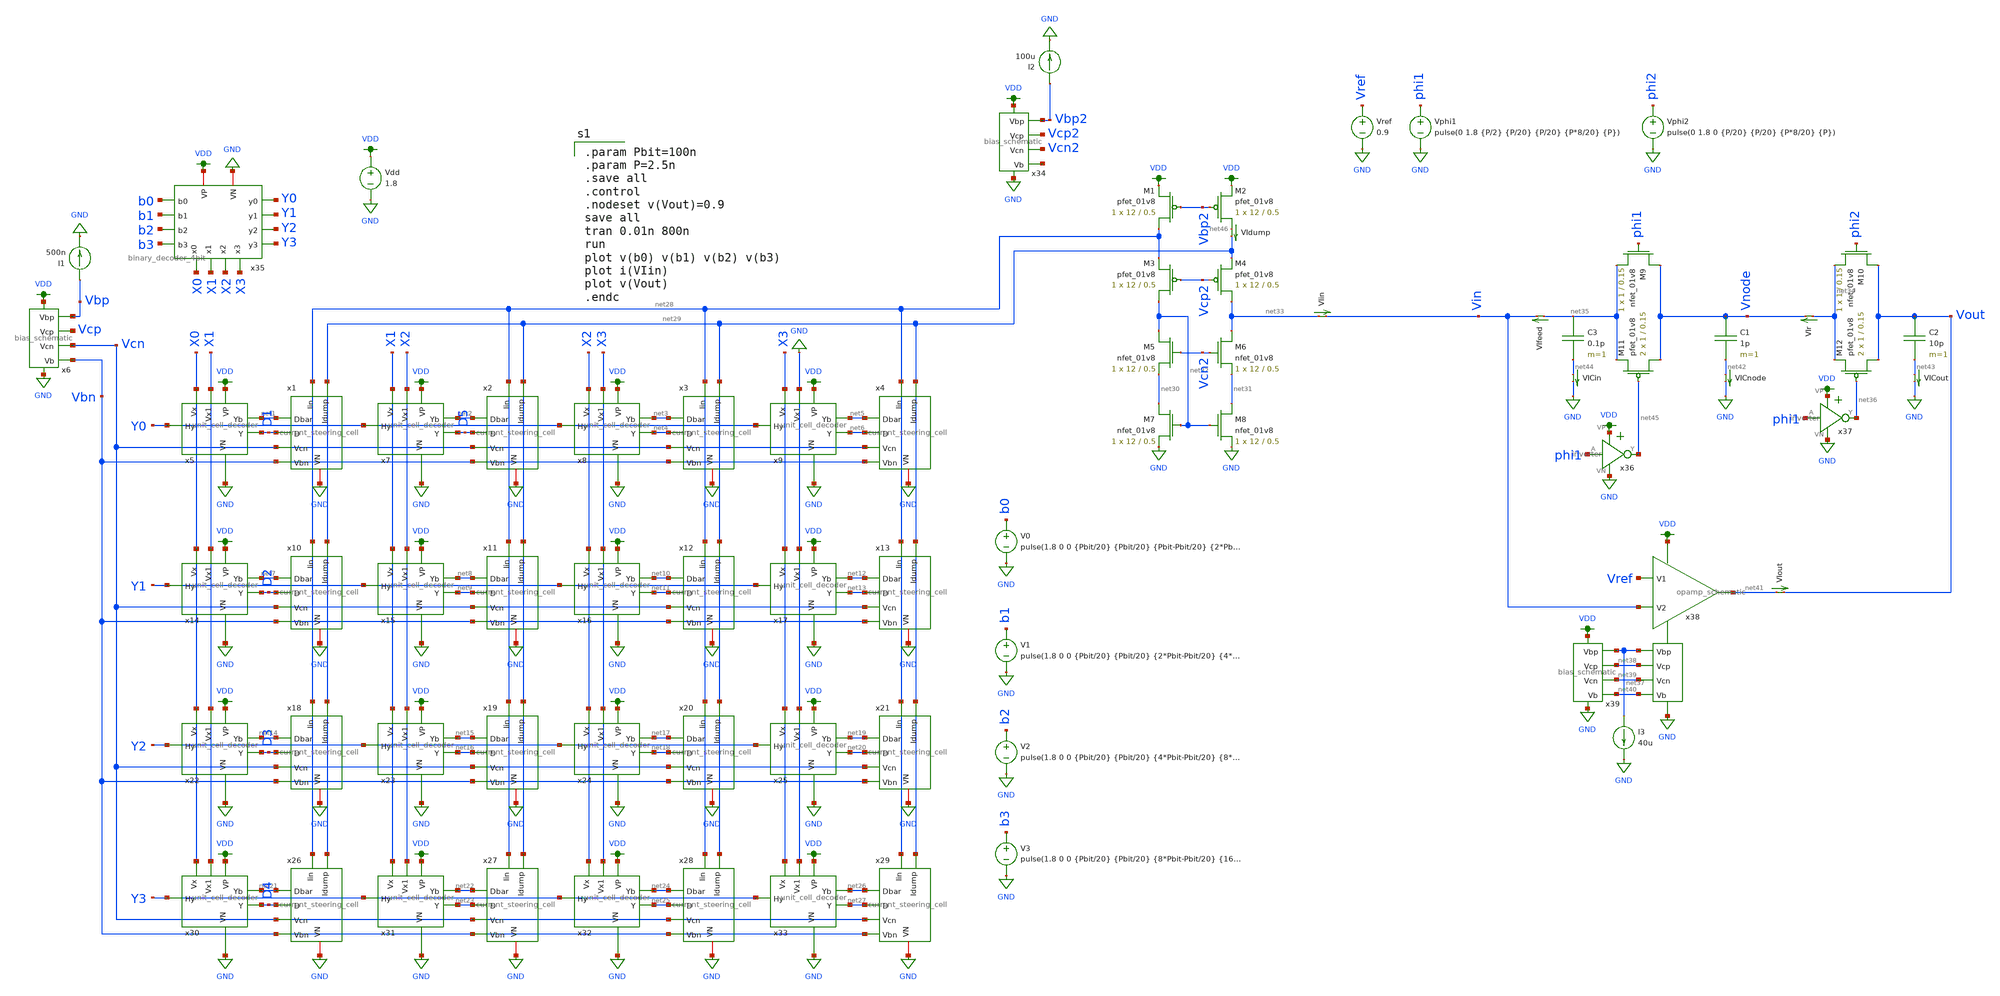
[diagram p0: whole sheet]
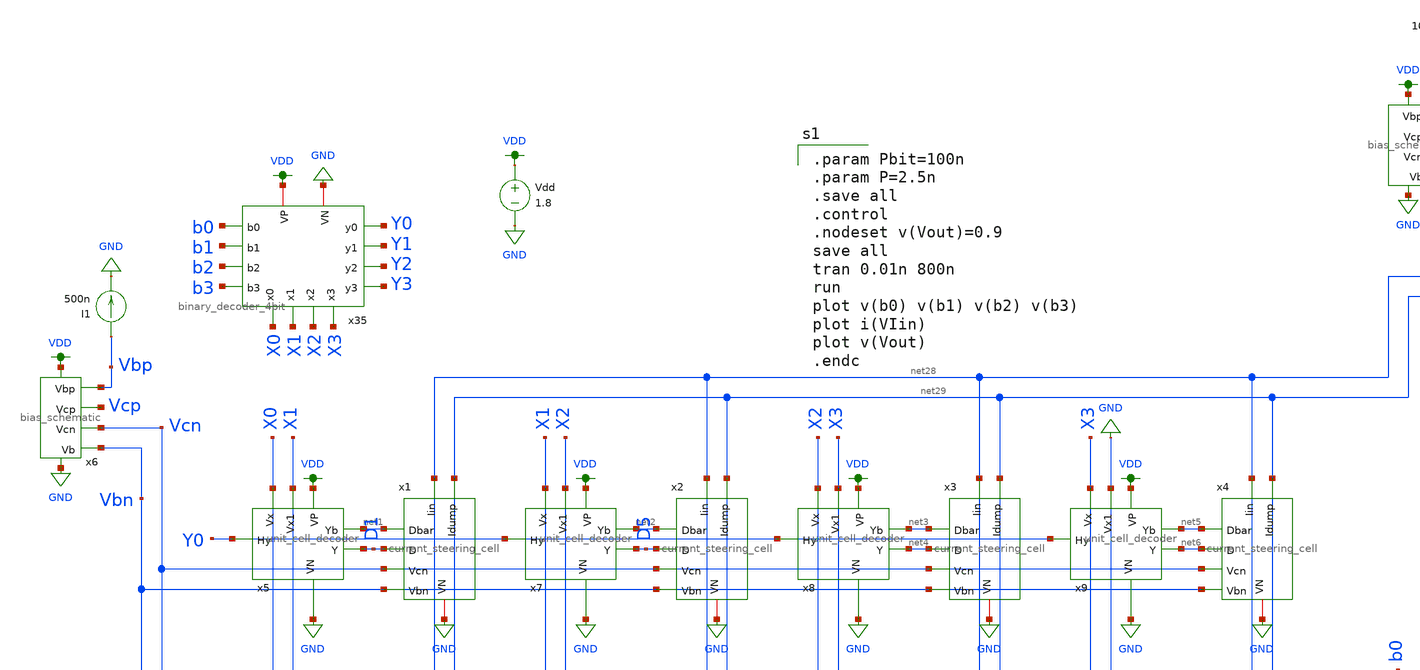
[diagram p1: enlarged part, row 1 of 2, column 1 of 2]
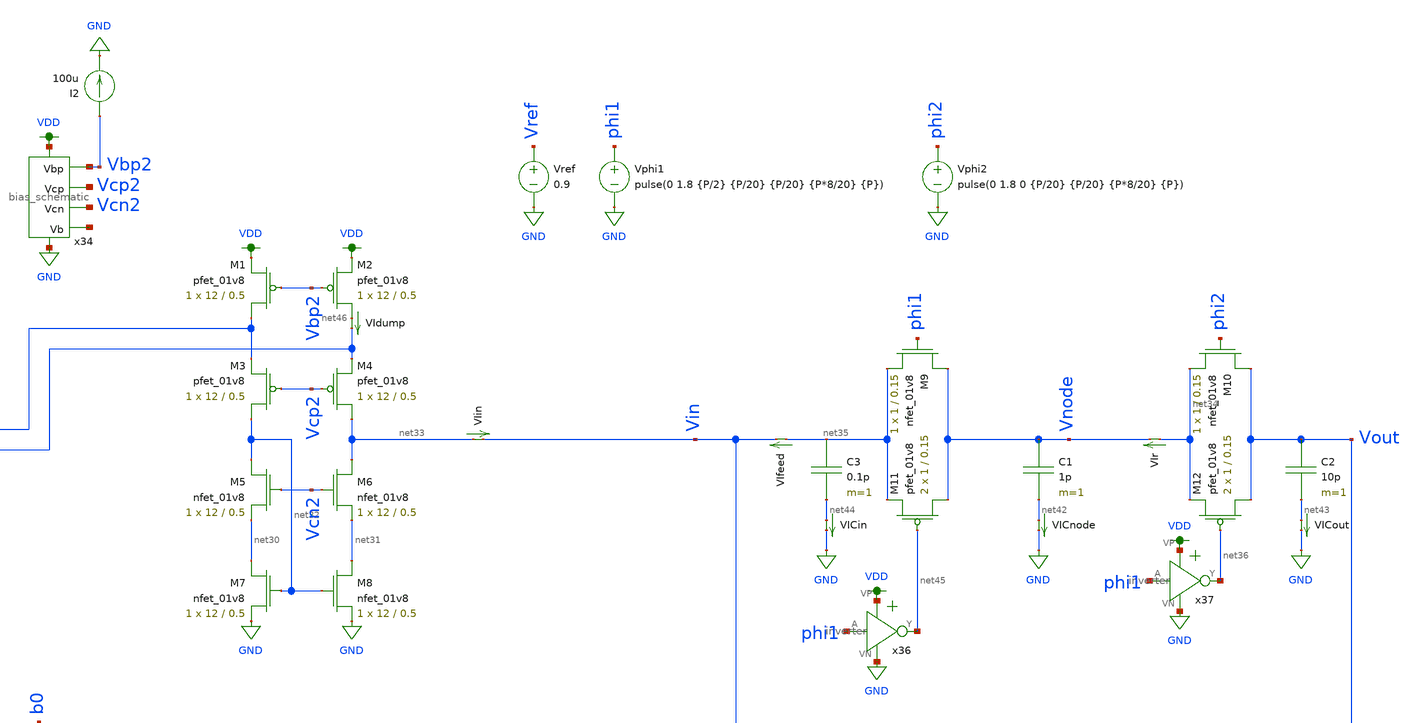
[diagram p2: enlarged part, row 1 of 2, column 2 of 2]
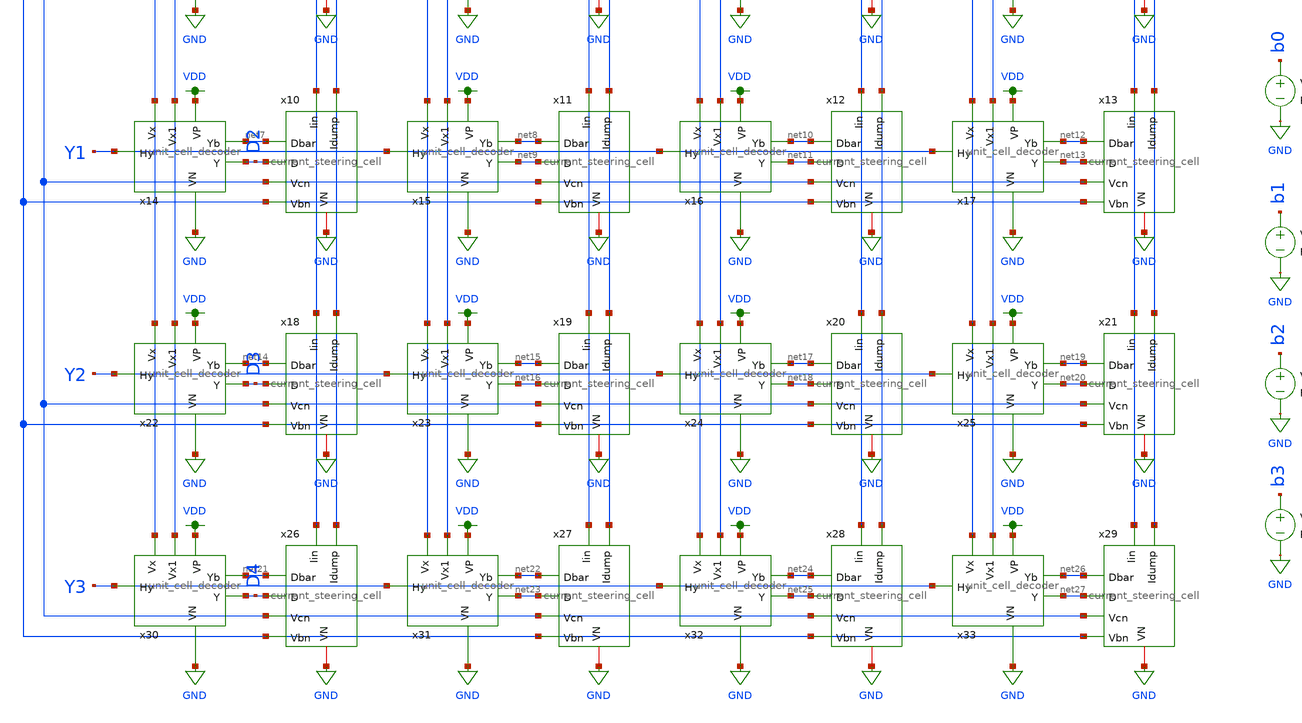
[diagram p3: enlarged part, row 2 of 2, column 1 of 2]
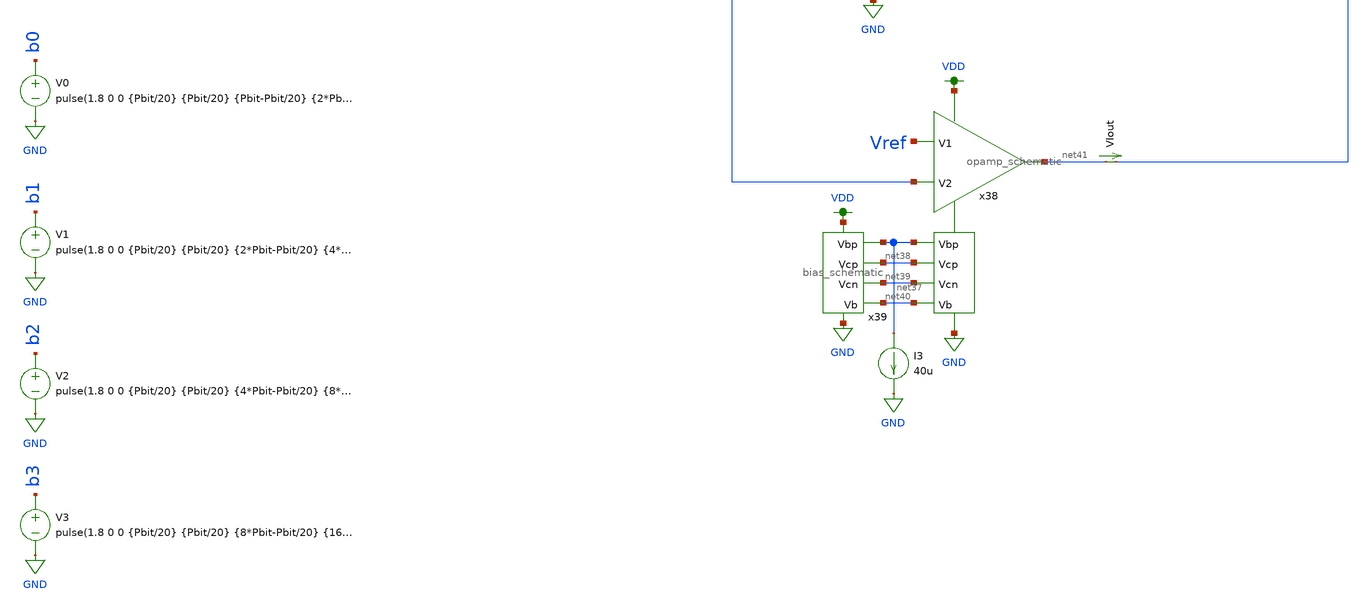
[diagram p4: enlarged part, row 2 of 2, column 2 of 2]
** sch_path: xschem/current_steering_testbenches/current_steering_testbench_transient_sciv.sch
**.subckt current_steering_testbench_transient_sciv
V1 b1 GND pulse(1.8 0 0 {Pbit/20} {Pbit/20} {2*Pbit-Pbit/20} {4*Pbit}
V2 b2 GND pulse(1.8 0 0 {Pbit/20} {Pbit/20} {4*Pbit-Pbit/20} {8*Pbit}
V3 b3 GND pulse(1.8 0 0 {Pbit/20} {Pbit/20} {8*Pbit-Pbit/20} {16*Pbit}
I1 Vbp GND 500n
VIin net33 Vin 0
.save i(viin)
Vdd VDD GND 1.8
XM1 net28 Vbp2 VDD VDD sky130_fd_pr__pfet_01v8 L=0.5 W=12 nf=1 ad='int((nf+1)/2) * W/nf * 0.29' as='int((nf+2)/2) * W/nf * 0.29'
+ pd='2*int((nf+1)/2) * (W/nf + 0.29)' ps='2*int((nf+2)/2) * (W/nf + 0.29)' nrd='0.29 / W' nrs='0.29 / W'
+ sa=0 sb=0 sd=0 mult=1 m=1
XM2 net46 Vbp2 VDD VDD sky130_fd_pr__pfet_01v8 L=0.5 W=12 nf=1 ad='int((nf+1)/2) * W/nf * 0.29' as='int((nf+2)/2) * W/nf * 0.29'
+ pd='2*int((nf+1)/2) * (W/nf + 0.29)' ps='2*int((nf+2)/2) * (W/nf + 0.29)' nrd='0.29 / W' nrs='0.29 / W'
+ sa=0 sb=0 sd=0 mult=1 m=1
XM3 net32 Vcp2 net28 VDD sky130_fd_pr__pfet_01v8 L=0.5 W=12 nf=1 ad='int((nf+1)/2) * W/nf * 0.29' as='int((nf+2)/2) * W/nf * 0.29'
+ pd='2*int((nf+1)/2) * (W/nf + 0.29)' ps='2*int((nf+2)/2) * (W/nf + 0.29)' nrd='0.29 / W' nrs='0.29 / W'
+ sa=0 sb=0 sd=0 mult=1 m=1
XM4 net33 Vcp2 net29 VDD sky130_fd_pr__pfet_01v8 L=0.5 W=12 nf=1 ad='int((nf+1)/2) * W/nf * 0.29' as='int((nf+2)/2) * W/nf * 0.29'
+ pd='2*int((nf+1)/2) * (W/nf + 0.29)' ps='2*int((nf+2)/2) * (W/nf + 0.29)' nrd='0.29 / W' nrs='0.29 / W'
+ sa=0 sb=0 sd=0 mult=1 m=1
V0 b0 GND pulse(1.8 0 0 {Pbit/20} {Pbit/20} {Pbit-Pbit/20} {2*Pbit}
x5 X0 X1 Y0 VDD GND net1 D1 unit_cell_decoder
x7 X1 X2 Y0 VDD GND net2 D5 unit_cell_decoder
x8 X2 X3 Y0 VDD GND net3 net4 unit_cell_decoder
x9 X3 GND Y0 VDD GND net5 net6 unit_cell_decoder
x14 X0 X1 Y1 VDD GND net7 D2 unit_cell_decoder
x15 X1 X2 Y1 VDD GND net8 net9 unit_cell_decoder
x16 X2 X3 Y1 VDD GND net10 net11 unit_cell_decoder
x17 X3 GND Y1 VDD GND net12 net13 unit_cell_decoder
x22 X0 X1 Y2 VDD GND net14 D3 unit_cell_decoder
x23 X1 X2 Y2 VDD GND net15 net16 unit_cell_decoder
x24 X2 X3 Y2 VDD GND net17 net18 unit_cell_decoder
x25 X3 GND Y2 VDD GND net19 net20 unit_cell_decoder
x30 X0 X1 Y3 VDD GND net21 D4 unit_cell_decoder
x31 X1 X2 Y3 VDD GND net22 net23 unit_cell_decoder
x32 X2 X3 Y3 VDD GND net24 net25 unit_cell_decoder
x33 X3 GND Y3 VDD GND net26 net27 unit_cell_decoder
x1 net28 net29 net1 D1 Vcn Vbn GND current_steering_cell
x2 net28 net29 net2 D5 Vcn Vbn GND current_steering_cell
x3 net28 net29 net3 net4 Vcn Vbn GND current_steering_cell
x4 net28 net29 net5 net6 Vcn Vbn GND current_steering_cell
x10 net28 net29 net7 D2 Vcn Vbn GND current_steering_cell
x11 net28 net29 net8 net9 Vcn Vbn GND current_steering_cell
x12 net28 net29 net10 net11 Vcn Vbn GND current_steering_cell
x13 net28 net29 net12 net13 Vcn Vbn GND current_steering_cell
x18 net28 net29 net14 D3 Vcn Vbn GND current_steering_cell
x19 net28 net29 net15 net16 Vcn Vbn GND current_steering_cell
x20 net28 net29 net17 net18 Vcn Vbn GND current_steering_cell
x21 net28 net29 net19 net20 Vcn Vbn GND current_steering_cell
x26 net28 net29 net21 D4 Vcn Vbn GND current_steering_cell
x27 net28 net29 net22 net23 Vcn Vbn GND current_steering_cell
x28 net28 net29 net24 net25 Vcn Vbn GND current_steering_cell
x29 net28 net29 net26 net27 Vcn Vbn GND current_steering_cell
x6 VDD Vbp Vcp Vcn GND Vbn bias_schematic
XM5 net32 Vcn2 net30 GND sky130_fd_pr__nfet_01v8 L=0.5 W=12 nf=1 ad='int((nf+1)/2) * W/nf * 0.29' as='int((nf+2)/2) * W/nf * 0.29'
+ pd='2*int((nf+1)/2) * (W/nf + 0.29)' ps='2*int((nf+2)/2) * (W/nf + 0.29)' nrd='0.29 / W' nrs='0.29 / W'
+ sa=0 sb=0 sd=0 mult=1 m=1
XM6 net33 Vcn2 net31 GND sky130_fd_pr__nfet_01v8 L=0.5 W=12 nf=1 ad='int((nf+1)/2) * W/nf * 0.29' as='int((nf+2)/2) * W/nf * 0.29'
+ pd='2*int((nf+1)/2) * (W/nf + 0.29)' ps='2*int((nf+2)/2) * (W/nf + 0.29)' nrd='0.29 / W' nrs='0.29 / W'
+ sa=0 sb=0 sd=0 mult=1 m=1
XM7 net30 net32 GND GND sky130_fd_pr__nfet_01v8 L=0.5 W=12 nf=1 ad='int((nf+1)/2) * W/nf * 0.29' as='int((nf+2)/2) * W/nf * 0.29'
+ pd='2*int((nf+1)/2) * (W/nf + 0.29)' ps='2*int((nf+2)/2) * (W/nf + 0.29)' nrd='0.29 / W' nrs='0.29 / W'
+ sa=0 sb=0 sd=0 mult=1 m=1
XM8 net31 net32 GND GND sky130_fd_pr__nfet_01v8 L=0.5 W=12 nf=1 ad='int((nf+1)/2) * W/nf * 0.29' as='int((nf+2)/2) * W/nf * 0.29'
+ pd='2*int((nf+1)/2) * (W/nf + 0.29)' ps='2*int((nf+2)/2) * (W/nf + 0.29)' nrd='0.29 / W' nrs='0.29 / W'
+ sa=0 sb=0 sd=0 mult=1 m=1
VIdump net46 net29 0
.save i(vidump)
I2 Vbp2 GND 100u
x34 VDD Vbp2 Vcp2 Vcn2 GND net47 bias_schematic
x35 Y0 X0 X1 Y1 VDD b0 b1 X2 Y2 b2 b3 GND Y3 X3 binary_decoder_4bit
C1 Vnode net42 1p m=1
XM9 Vnode phi1 net35 GND sky130_fd_pr__nfet_01v8 L=0.15 W=1 nf=1 ad='int((nf+1)/2) * W/nf * 0.29' as='int((nf+2)/2) * W/nf * 0.29'
+ pd='2*int((nf+1)/2) * (W/nf + 0.29)' ps='2*int((nf+2)/2) * (W/nf + 0.29)' nrd='0.29 / W' nrs='0.29 / W'
+ sa=0 sb=0 sd=0 mult=1 m=1
XM10 Vout phi2 net34 GND sky130_fd_pr__nfet_01v8 L=0.15 W=1 nf=1 ad='int((nf+1)/2) * W/nf * 0.29' as='int((nf+2)/2) * W/nf * 0.29'
+ pd='2*int((nf+1)/2) * (W/nf + 0.29)' ps='2*int((nf+2)/2) * (W/nf + 0.29)' nrd='0.29 / W' nrs='0.29 / W'
+ sa=0 sb=0 sd=0 mult=1 m=1
C2 Vout net43 10p m=1
XM11 Vnode net45 net35 VDD sky130_fd_pr__pfet_01v8 L=0.15 W=1 nf=1 ad='int((nf+1)/2) * W/nf * 0.29' as='int((nf+2)/2) * W/nf * 0.29'
+ pd='2*int((nf+1)/2) * (W/nf + 0.29)' ps='2*int((nf+2)/2) * (W/nf + 0.29)' nrd='0.29 / W' nrs='0.29 / W'
+ sa=0 sb=0 sd=0 mult=2 m=2
XM12 Vout net36 net34 VDD sky130_fd_pr__pfet_01v8 L=0.15 W=1 nf=1 ad='int((nf+1)/2) * W/nf * 0.29' as='int((nf+2)/2) * W/nf * 0.29'
+ pd='2*int((nf+1)/2) * (W/nf + 0.29)' ps='2*int((nf+2)/2) * (W/nf + 0.29)' nrd='0.29 / W' nrs='0.29 / W'
+ sa=0 sb=0 sd=0 mult=2 m=2
x36 VDD phi1 net45 GND inverter
x37 VDD phi1 net36 GND inverter
C3 net35 net44 0.1p m=1
x38 VDD net37 net38 net41 Vref Vin net39 net40 GND opamp_schematic
x39 VDD net37 net38 net39 GND net40 bias_schematic
I3 net37 GND 40u
VIr net34 Vnode 0
.save i(vir)
VIout net41 Vout 0
.save i(viout)
VICnode net42 GND 0
.save i(vicnode)
VICout net43 GND 0
.save i(vicout)
VICin net44 GND 0
.save i(vicin)
VIfeed net35 Vin 0
.save i(vifeed)
Vphi1 phi1 GND pulse(0 1.8 {P/2} {P/20} {P/20} {P*8/20} {P})
Vphi2 phi2 GND pulse(0 1.8 0 {P/20} {P/20} {P*8/20} {P})
Vref Vref GND 0.9
**** begin user architecture code

.option wnflag=1
.param MC_SWITCH=0.0
.lib ~/skywater/skywater-pdk/libraries/sky130_fd_pr_ngspice/latest/models/sky130.lib.spice tt


.param Pbit=100n
.param P=2.5n
.save all
.control
.nodeset v(Vout)=0.9
save all
tran 0.01n 800n
run
plot v(b0) v(b1) v(b2) v(b3)
plot i(VIin)
plot v(Vout)
.endc

**** end user architecture code
**.ends
.GLOBAL GND
.GLOBAL VDD
.end
